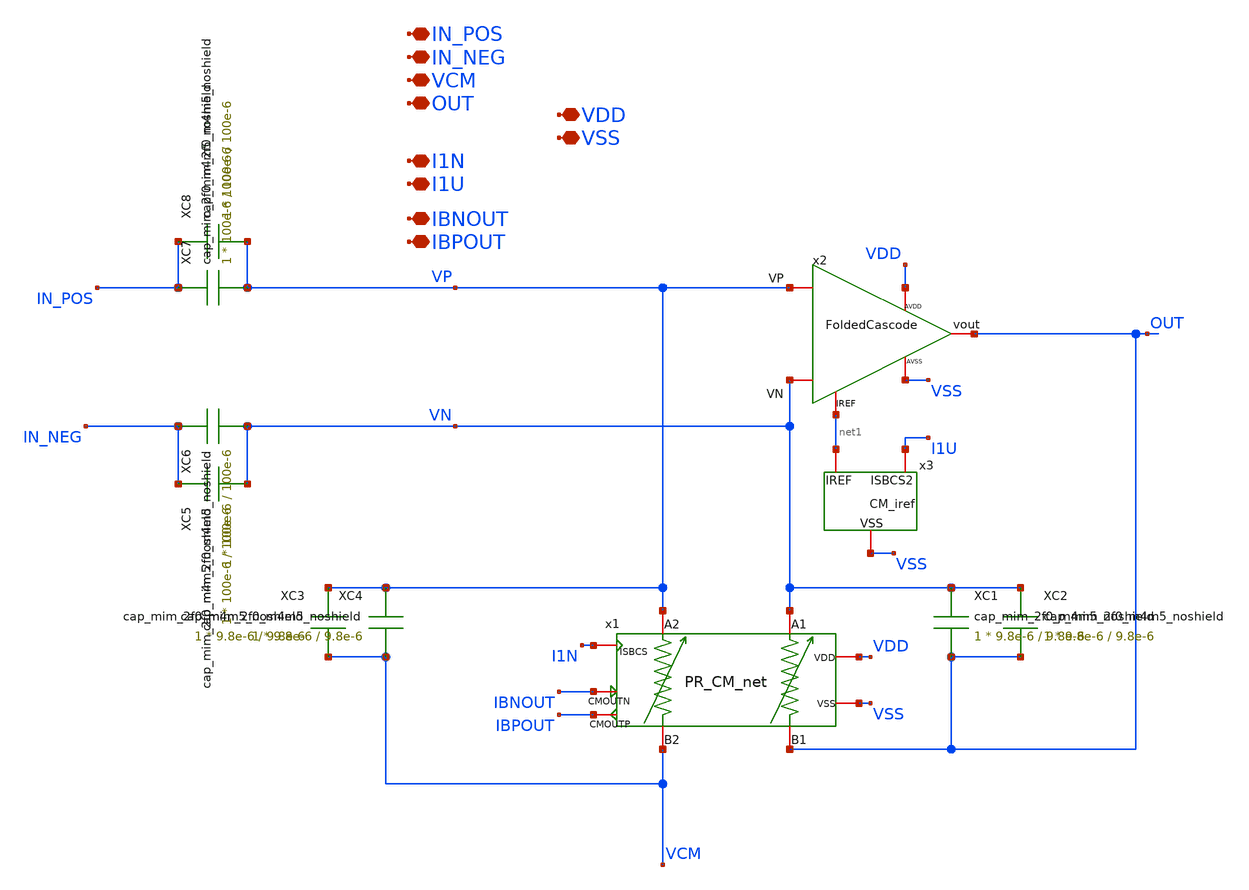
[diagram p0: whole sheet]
** sch_path: TIA_Filter/Filter_TOP.sch
**.subckt Filter_TOP IN_POS IN_NEG I1N I1U VCM OUT IBNOUT IBPOUT VDD VSS
*.iopin IN_POS
*.iopin IN_NEG
*.iopin I1N
*.iopin I1U
*.iopin VCM
*.iopin OUT
*.iopin IBNOUT
*.iopin IBPOUT
*.iopin VDD
*.iopin VSS
XC1 VN OUT cap_mim_2f0_m4m5_noshield c_width=9.8e-6 c_length=9.8e-6 m=1
XC4 VP VCM cap_mim_2f0_m4m5_noshield c_width=9.8e-6 c_length=9.8e-6 m=1
XC7 IN_POS VP cap_mim_2f0_m4m5_noshield c_width=100e-6 c_length=100e-6 m=1
XC6 IN_NEG VN cap_mim_2f0_m4m5_noshield c_width=100e-6 c_length=100e-6 m=1
x2 VP VN OUT net1 VDD VSS FoldedCascode
x3 I1U net1 VSS CM_iref
x1 I1N VN VP VCM OUT IBNOUT IBPOUT VDD VSS PR_CM_net
XC2 VN OUT cap_mim_2f0_m4m5_noshield c_width=9.8e-6 c_length=9.8e-6 m=1
XC3 VP VCM cap_mim_2f0_m4m5_noshield c_width=9.8e-6 c_length=9.8e-6 m=1
XC5 IN_NEG VN cap_mim_2f0_m4m5_noshield c_width=100e-6 c_length=100e-6 m=1
XC8 IN_POS VP cap_mim_2f0_m4m5_noshield c_width=100e-6 c_length=100e-6 m=1
**.ends
.end
